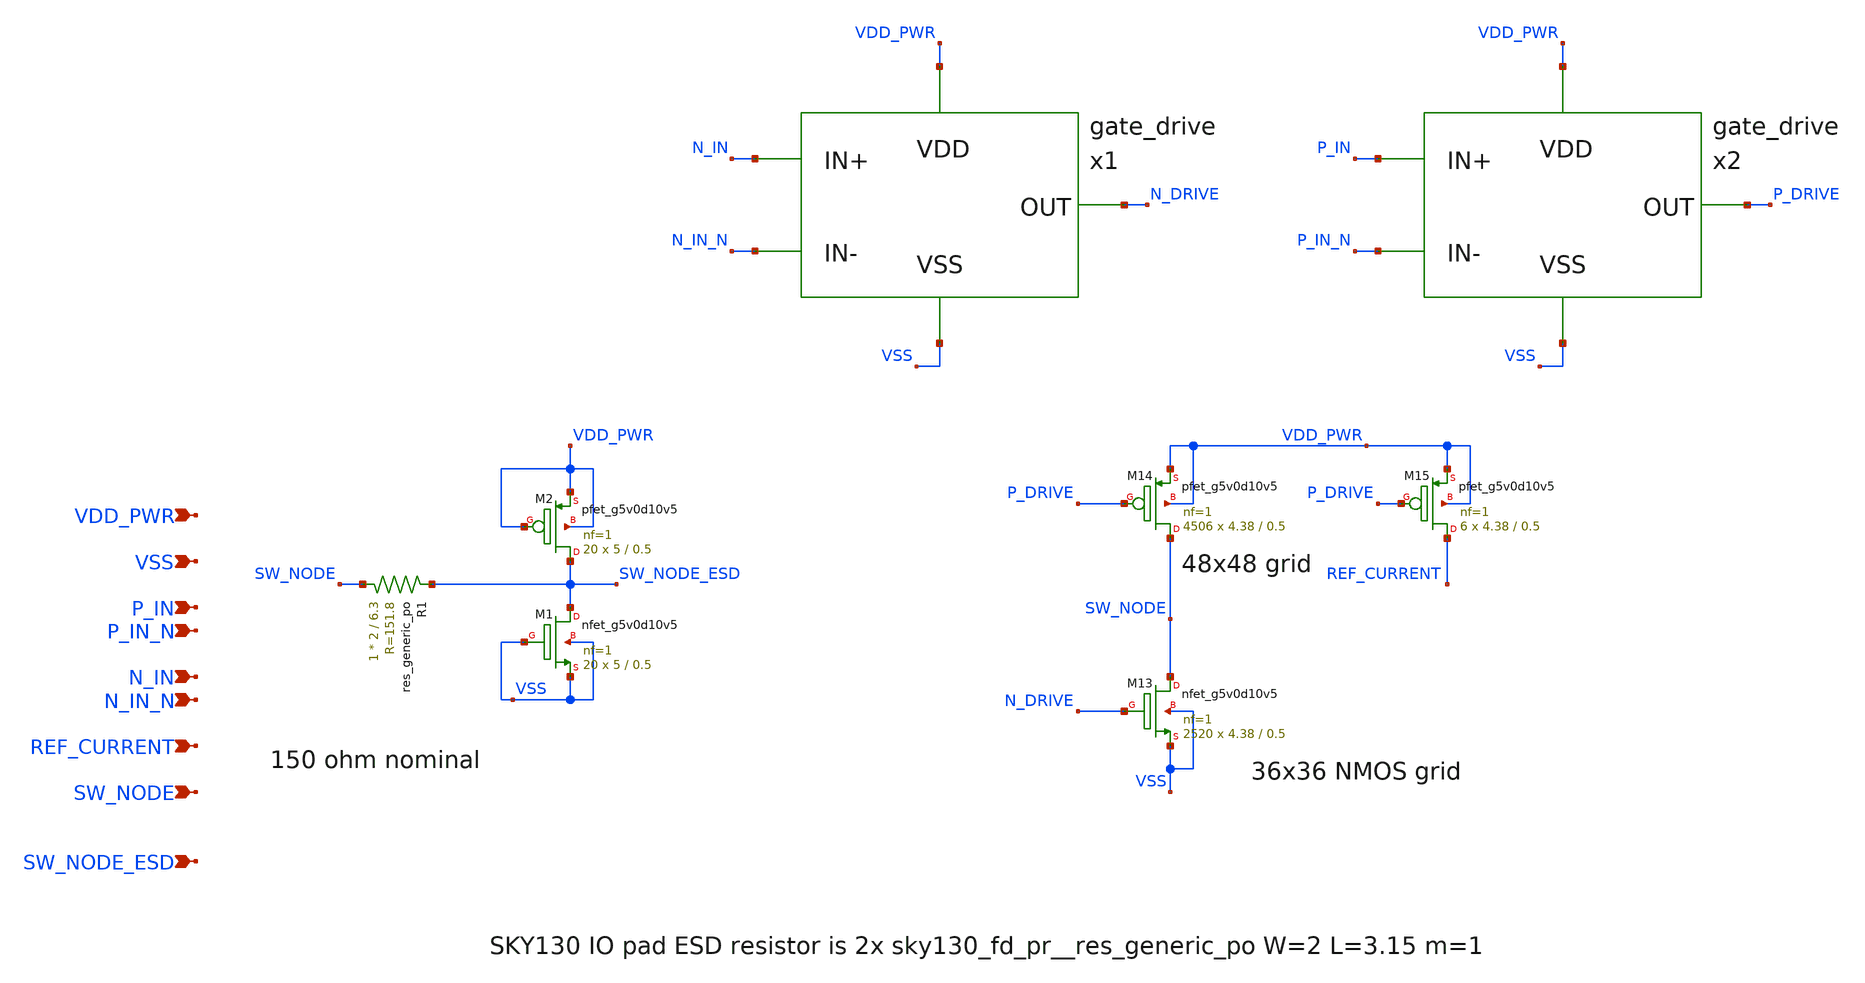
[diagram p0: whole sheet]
** sch_path: design/power-stage/power_stage.sch
**.subckt power_stage N_IN VSS P_IN P_IN_N N_IN_N VDD_PWR REF_CURRENT SW_NODE SW_NODE_ESD
*.ipin N_IN
*.ipin VSS
*.ipin P_IN
*.ipin P_IN_N
*.ipin N_IN_N
*.ipin VDD_PWR
*.ipin REF_CURRENT
*.ipin SW_NODE
*.ipin SW_NODE_ESD
XM13 SW_NODE N_DRIVE VSS VSS sky130_fd_pr__nfet_g5v0d10v5 L=0.5 W=4.38 nf=1 ad='int((nf+1)/2) * W/nf * 0.29'
+ as='int((nf+2)/2) * W/nf * 0.29' pd='2*int((nf+1)/2) * (W/nf + 0.29)' ps='2*int((nf+2)/2) * (W/nf + 0.29)'
+ nrd='0.29 / W' nrs='0.29 / W' sa=0 sb=0 sd=0 mult=2520 m=2520
XM14 SW_NODE P_DRIVE VDD_PWR VDD_PWR sky130_fd_pr__pfet_g5v0d10v5 L=0.5 W=4.38 nf=1 ad='int((nf+1)/2) * W/nf * 0.29'
+ as='int((nf+2)/2) * W/nf * 0.29' pd='2*int((nf+1)/2) * (W/nf + 0.29)' ps='2*int((nf+2)/2) * (W/nf + 0.29)'
+ nrd='0.29 / W' nrs='0.29 / W' sa=0 sb=0 sd=0 mult=4506 m=4506
XM15 REF_CURRENT P_DRIVE VDD_PWR VDD_PWR sky130_fd_pr__pfet_g5v0d10v5 L=0.5 W=4.38 nf=1 ad='int((nf+1)/2) * W/nf * 0.29'
+ as='int((nf+2)/2) * W/nf * 0.29' pd='2*int((nf+1)/2) * (W/nf + 0.29)' ps='2*int((nf+2)/2) * (W/nf + 0.29)'
+ nrd='0.29 / W' nrs='0.29 / W' sa=0 sb=0 sd=0 mult=6 m=6
x1 N_IN N_IN_N VDD_PWR VSS N_DRIVE gate_drive
x2 P_IN P_IN_N VDD_PWR VSS P_DRIVE gate_drive
XM1 SW_NODE_ESD VSS VSS VSS sky130_fd_pr__nfet_g5v0d10v5 L=0.5 W=5 nf=1 ad='int((nf+1)/2) * W/nf * 0.29'
+ as='int((nf+2)/2) * W/nf * 0.29' pd='2*int((nf+1)/2) * (W/nf + 0.29)' ps='2*int((nf+2)/2) * (W/nf + 0.29)'
+ nrd='0.29 / W' nrs='0.29 / W' sa=0 sb=0 sd=0 mult=20 m=20
XM2 SW_NODE_ESD VDD_PWR VDD_PWR VDD_PWR sky130_fd_pr__pfet_g5v0d10v5 L=0.5 W=5 nf=1 ad='int((nf+1)/2) * W/nf * 0.29'
+ as='int((nf+2)/2) * W/nf * 0.29' pd='2*int((nf+1)/2) * (W/nf + 0.29)' ps='2*int((nf+2)/2) * (W/nf + 0.29)'
+ nrd='0.29 / W' nrs='0.29 / W' sa=0 sb=0 sd=0 mult=20 m=20
XR1 SW_NODE SW_NODE_ESD sky130_fd_pr__res_generic_po W=2 L=6.3 m=1
**.ends

* expanding   symbol:  design/power-stage/gate_drive.sym # of pins=5
** sym_path: design/power-stage/gate_drive.sym
** sch_path: design/power-stage/gate_drive.sch
.subckt gate_drive IN_P IN_M VDD VSS OUT
*.ipin OUT
*.ipin VSS
*.ipin IN_P
*.ipin IN_M
*.ipin VDD
XM1 net1 IN_P VSS VSS sky130_fd_pr__nfet_g5v0d10v5 L=0.5 W=1 nf=1 ad='int((nf+1)/2) * W/nf * 0.29' as='int((nf+2)/2) * W/nf * 0.29'
+ pd='2*int((nf+1)/2) * (W/nf + 0.29)' ps='2*int((nf+2)/2) * (W/nf + 0.29)' nrd='0.29 / W' nrs='0.29 / W'
+ sa=0 sb=0 sd=0 mult=1 m=1
XM2 net1 S1_N VDD VDD sky130_fd_pr__pfet_g5v0d10v5 L=0.5 W=2 nf=1 ad='int((nf+1)/2) * W/nf * 0.29' as='int((nf+2)/2) * W/nf * 0.29'
+ pd='2*int((nf+1)/2) * (W/nf + 0.29)' ps='2*int((nf+2)/2) * (W/nf + 0.29)' nrd='0.29 / W' nrs='0.29 / W'
+ sa=0 sb=0 sd=0 mult=1 m=1
XM3 S1_N IN_M VSS VSS sky130_fd_pr__nfet_g5v0d10v5 L=0.5 W=1 nf=1 ad='int((nf+1)/2) * W/nf * 0.29' as='int((nf+2)/2) * W/nf * 0.29'
+ pd='2*int((nf+1)/2) * (W/nf + 0.29)' ps='2*int((nf+2)/2) * (W/nf + 0.29)' nrd='0.29 / W' nrs='0.29 / W'
+ sa=0 sb=0 sd=0 mult=1 m=1
XM4 S1_N net1 VDD VDD sky130_fd_pr__pfet_g5v0d10v5 L=0.5 W=2 nf=1 ad='int((nf+1)/2) * W/nf * 0.29' as='int((nf+2)/2) * W/nf * 0.29'
+ pd='2*int((nf+1)/2) * (W/nf + 0.29)' ps='2*int((nf+2)/2) * (W/nf + 0.29)' nrd='0.29 / W' nrs='0.29 / W'
+ sa=0 sb=0 sd=0 mult=1 m=1
XM5 S2_N S1_N VDD VDD sky130_fd_pr__pfet_g5v0d10v5 L=0.5 W=10 nf=1 ad='int((nf+1)/2) * W/nf * 0.29' as='int((nf+2)/2) * W/nf * 0.29'
+ pd='2*int((nf+1)/2) * (W/nf + 0.29)' ps='2*int((nf+2)/2) * (W/nf + 0.29)' nrd='0.29 / W' nrs='0.29 / W'
+ sa=0 sb=0 sd=0 mult=1 m=1
XM6 S2_N S1_N VSS VSS sky130_fd_pr__nfet_g5v0d10v5 L=0.5 W=5 nf=1 ad='int((nf+1)/2) * W/nf * 0.29' as='int((nf+2)/2) * W/nf * 0.29'
+ pd='2*int((nf+1)/2) * (W/nf + 0.29)' ps='2*int((nf+2)/2) * (W/nf + 0.29)' nrd='0.29 / W' nrs='0.29 / W'
+ sa=0 sb=0 sd=0 mult=1 m=1
XM7 S3_N S2_N VDD VDD sky130_fd_pr__pfet_g5v0d10v5 L=0.5 W=20 nf=1 ad='int((nf+1)/2) * W/nf * 0.29' as='int((nf+2)/2) * W/nf * 0.29'
+ pd='2*int((nf+1)/2) * (W/nf + 0.29)' ps='2*int((nf+2)/2) * (W/nf + 0.29)' nrd='0.29 / W' nrs='0.29 / W'
+ sa=0 sb=0 sd=0 mult=4 m=4
XM8 S3_N S2_N VSS VSS sky130_fd_pr__nfet_g5v0d10v5 L=0.5 W=20 nf=1 ad='int((nf+1)/2) * W/nf * 0.29' as='int((nf+2)/2) * W/nf * 0.29'
+ pd='2*int((nf+1)/2) * (W/nf + 0.29)' ps='2*int((nf+2)/2) * (W/nf + 0.29)' nrd='0.29 / W' nrs='0.29 / W'
+ sa=0 sb=0 sd=0 mult=2 m=2
XM9 S4_N S3_N VDD VDD sky130_fd_pr__pfet_g5v0d10v5 L=0.5 W=20 nf=1 ad='int((nf+1)/2) * W/nf * 0.29' as='int((nf+2)/2) * W/nf * 0.29'
+ pd='2*int((nf+1)/2) * (W/nf + 0.29)' ps='2*int((nf+2)/2) * (W/nf + 0.29)' nrd='0.29 / W' nrs='0.29 / W'
+ sa=0 sb=0 sd=0 mult=22 m=22
XM10 S4_N S3_N VSS VSS sky130_fd_pr__nfet_g5v0d10v5 L=0.5 W=20 nf=1 ad='int((nf+1)/2) * W/nf * 0.29'
+ as='int((nf+2)/2) * W/nf * 0.29' pd='2*int((nf+1)/2) * (W/nf + 0.29)' ps='2*int((nf+2)/2) * (W/nf + 0.29)'
+ nrd='0.29 / W' nrs='0.29 / W' sa=0 sb=0 sd=0 mult=11 m=11
XM11 OUT S4_N VDD VDD sky130_fd_pr__pfet_g5v0d10v5 L=0.5 W=20 nf=1 ad='int((nf+1)/2) * W/nf * 0.29' as='int((nf+2)/2) * W/nf * 0.29'
+ pd='2*int((nf+1)/2) * (W/nf + 0.29)' ps='2*int((nf+2)/2) * (W/nf + 0.29)' nrd='0.29 / W' nrs='0.29 / W'
+ sa=0 sb=0 sd=0 mult=120 m=120
XM12 OUT S4_N VSS VSS sky130_fd_pr__nfet_g5v0d10v5 L=0.5 W=20 nf=1 ad='int((nf+1)/2) * W/nf * 0.29' as='int((nf+2)/2) * W/nf * 0.29'
+ pd='2*int((nf+1)/2) * (W/nf + 0.29)' ps='2*int((nf+2)/2) * (W/nf + 0.29)' nrd='0.29 / W' nrs='0.29 / W'
+ sa=0 sb=0 sd=0 mult=60 m=60
.ends

.end
